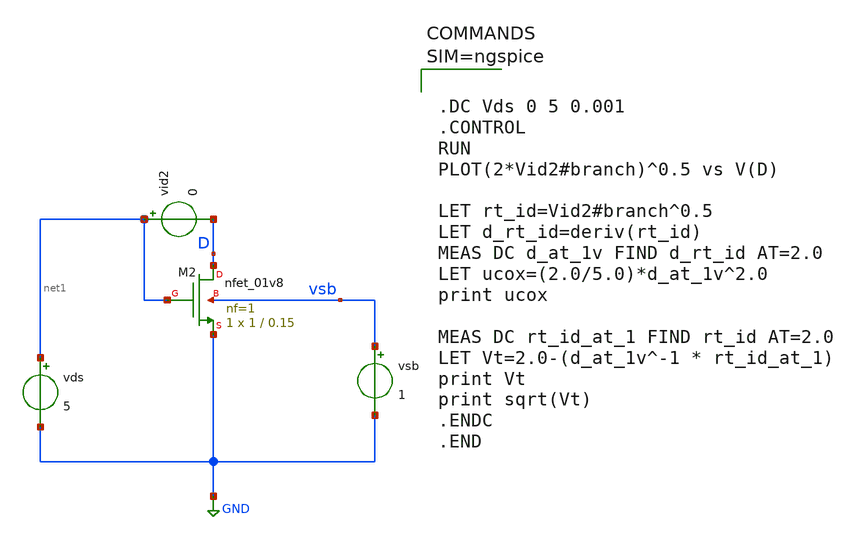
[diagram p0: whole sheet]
** sch_path: xschem/para_ex.sch
**.subckt para_ex
vsb vsb GND 1
vds net1 GND 5
vid2 net1 D 0
XM2 D net1 GND vsb sky130_fd_pr__nfet_01v8 L=0.15 W=1 nf=1 ad='int((1 + 1)/2) * 1 / 1 * 0.29' as='int((1 + 2)/2) * 1 / 1 * 0.29'
+ pd='2*int((1 + 1)/2) * (1 / 1 + 0.29)' ps='2*int((1 + 2)/2) * (1 / 1 + 0.29)' nrd='0.29 / 1 ' nrs='0.29 / 1 '
+ sa=0 sb=0 sd=0 mult=1 m=1
**** begin user architecture code

** opencircuitdesign pdks install
.lib $::SKYWATER_MODELS/sky130.lib.spice tt




.DC Vds 0 5 0.001
.CONTROL
RUN
PLOT(2*Vid2#branch)^0.5 vs V(D)

LET rt_id=Vid2#branch^0.5
LET d_rt_id=deriv(rt_id)
MEAS DC d_at_1v FIND d_rt_id AT=2.0
LET ucox=(2.0/5.0)*d_at_1v^2.0
print ucox

MEAS DC rt_id_at_1 FIND rt_id AT=2.0
LET Vt=2.0-(d_at_1v^-1 * rt_id_at_1)
print Vt
print sqrt(Vt)
.ENDC
.END



**** end user architecture code
**.ends
.GLOBAL GND
.end
